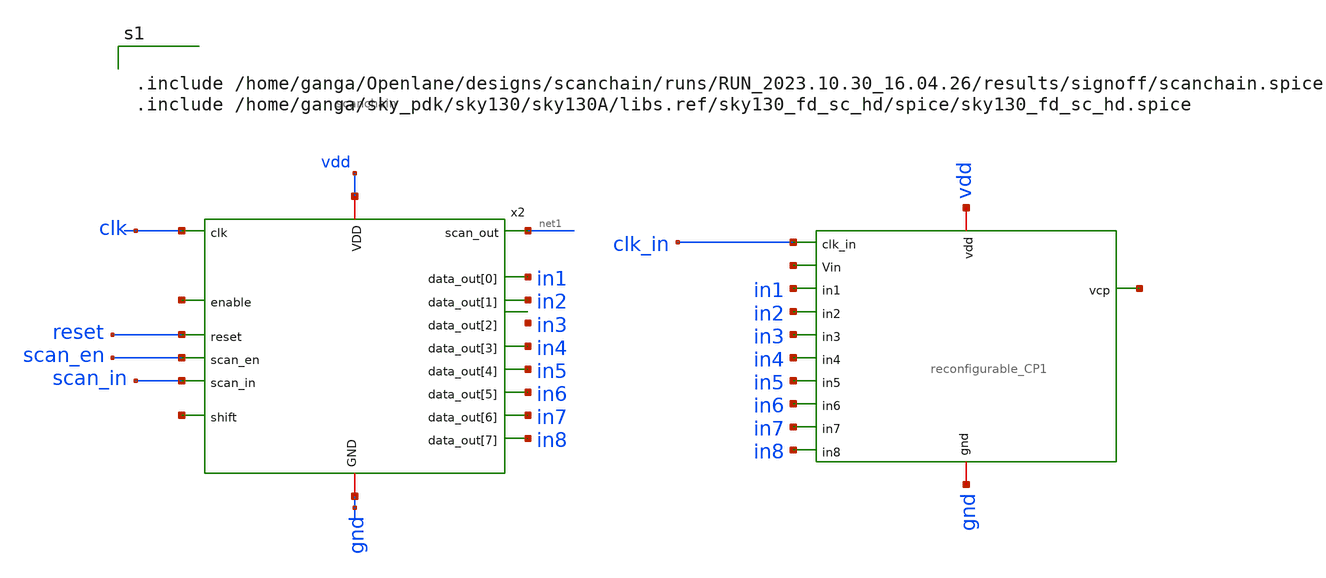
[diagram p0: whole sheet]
** sch_path: xschem/reconfigurable_CP_withScanchain.sch
**.subckt reconfigurable_CP_withScanchain
x2 clk reset net1 scan_en scan_in in5 in1 in6 in2 in7 in3 net2 in8 in4 vdd gnd net3 scanchain
x1 clk_in net4 net5 in1 in2 in3 in4 in5 in6 in7 in8 vdd gnd reconfigurable_CP1
**** begin user architecture code


.include /home/ganga/Openlane/designs/scanchain/runs/RUN_2023.10.30_16.04.26/results/signoff/scanchain.spice
.include /home/ganga/sky_pdk/sky130/sky130A/libs.ref/sky130_fd_sc_hd/spice/sky130_fd_sc_hd.spice


**** end user architecture code
**.ends
.end
